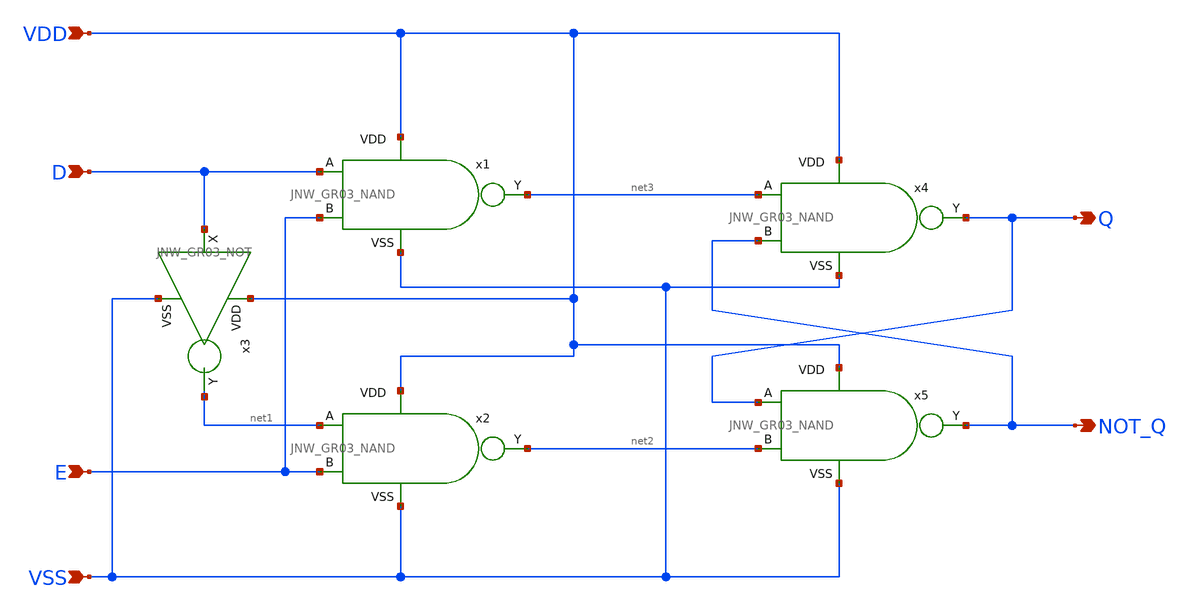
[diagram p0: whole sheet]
** sch_path: design/JNW_GR03_SKY130A/JNW_GR03_DLATCH.sch
**.subckt JNW_GR03_DLATCH VDD VSS E D Q NOT_Q
*.ipin VDD
*.ipin VSS
*.ipin E
*.ipin D
*.opin Q
*.opin NOT_Q
x1 VDD net3 D E VSS JNW_GR03_NAND
x2 VDD net2 net1 E VSS JNW_GR03_NAND
x3 VDD D net1 VSS JNW_GR03_NOT
x4 VDD Q net3 NOT_Q VSS JNW_GR03_NAND
x5 VDD NOT_Q Q net2 VSS JNW_GR03_NAND
**.ends
.end
